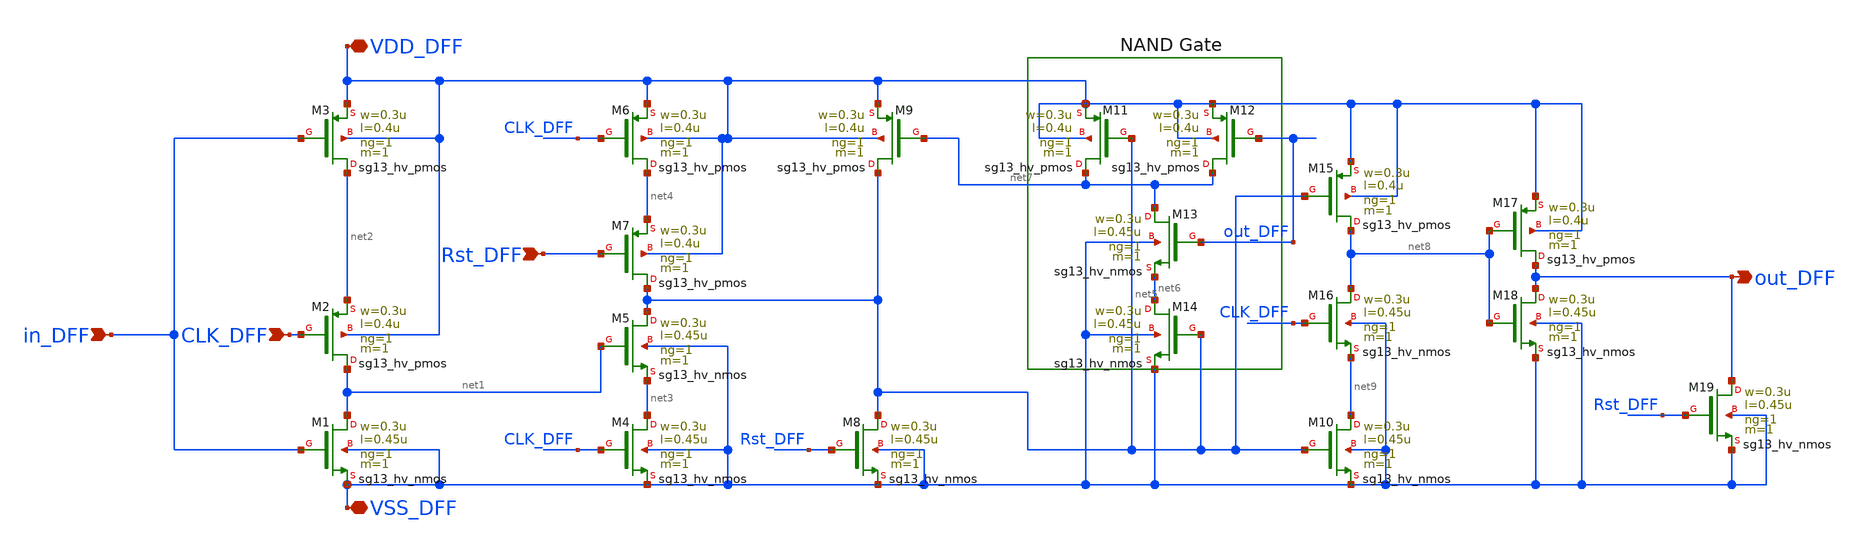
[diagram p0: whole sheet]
** sch_path: circuit_files/xschem_symbols/simp_DFF.sch
**.subckt simp_DFF in_DFF CLK_DFF Rst_DFF out_DFF VDD_DFF VSS_DFF
*.ipin in_DFF
*.ipin CLK_DFF
*.ipin Rst_DFF
*.opin out_DFF
*.iopin VDD_DFF
*.iopin VSS_DFF
XM1 net1 in_DFF VSS_DFF VSS_DFF sg13_hv_nmos w=0.3u l=0.45u ng=1 m=1 mm_ok=1
XM2 net1 CLK_DFF net2 VDD_DFF sg13_hv_pmos w=0.3u l=0.4u ng=1 m=1 mm_ok=1
XM3 net2 in_DFF VDD_DFF VDD_DFF sg13_hv_pmos w=0.3u l=0.4u ng=1 m=1 mm_ok=1
XM4 net3 CLK_DFF VSS_DFF VSS_DFF sg13_hv_nmos w=0.3u l=0.45u ng=1 m=1 mm_ok=1
XM5 net5 net1 net3 VSS_DFF sg13_hv_nmos w=0.3u l=0.45u ng=1 m=1 mm_ok=1
XM6 net4 CLK_DFF VDD_DFF VDD_DFF sg13_hv_pmos w=0.3u l=0.4u ng=1 m=1 mm_ok=1
XM7 net5 Rst_DFF net4 VDD_DFF sg13_hv_pmos w=0.3u l=0.4u ng=1 m=1 mm_ok=1
XM8 net5 Rst_DFF VSS_DFF VSS_DFF sg13_hv_nmos w=0.3u l=0.45u ng=1 m=1 mm_ok=1
XM9 net5 net7 VDD_DFF VDD_DFF sg13_hv_pmos w=0.3u l=0.4u ng=1 m=1 mm_ok=1
XM10 net9 net5 VSS_DFF VSS_DFF sg13_hv_nmos w=0.3u l=0.45u ng=1 m=1 mm_ok=1
XM11 net7 net5 VDD_DFF VDD_DFF sg13_hv_pmos w=0.3u l=0.4u ng=1 m=1 mm_ok=1
XM12 net7 out_DFF VDD_DFF VDD_DFF sg13_hv_pmos w=0.3u l=0.4u ng=1 m=1 mm_ok=1
XM13 net7 out_DFF net6 VSS_DFF sg13_hv_nmos w=0.3u l=0.45u ng=1 m=1 mm_ok=1
XM14 net6 net5 VSS_DFF VSS_DFF sg13_hv_nmos w=0.3u l=0.45u ng=1 m=1 mm_ok=1
XM15 net8 net5 VDD_DFF VDD_DFF sg13_hv_pmos w=0.3u l=0.4u ng=1 m=1 mm_ok=1
XM16 net8 CLK_DFF net9 VSS_DFF sg13_hv_nmos w=0.3u l=0.45u ng=1 m=1 mm_ok=1
XM17 out_DFF net8 VDD_DFF VDD_DFF sg13_hv_pmos w=0.3u l=0.4u ng=1 m=1 mm_ok=1
XM18 out_DFF net8 VSS_DFF VSS_DFF sg13_hv_nmos w=0.3u l=0.45u ng=1 m=1 mm_ok=1
XM19 out_DFF Rst_DFF VSS_DFF VSS_DFF sg13_hv_nmos w=0.3u l=0.45u ng=1 m=1 mm_ok=1
**.ends
.end
